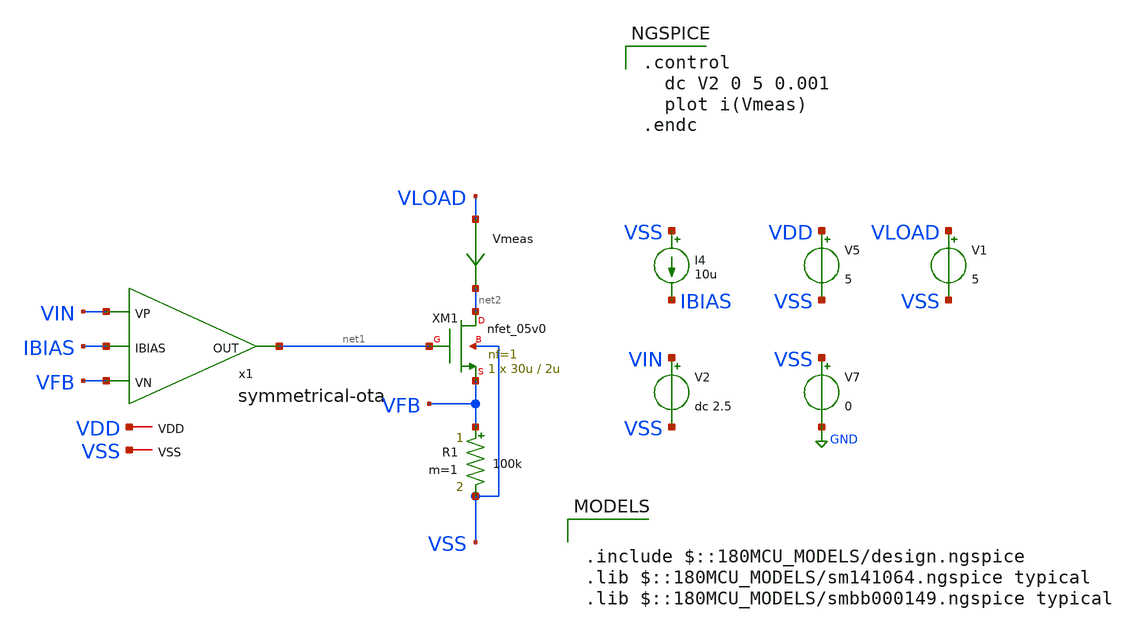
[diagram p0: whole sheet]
** sch_path: designs/vi-converter/vi-converter.sch
**.subckt vi-converter
x1 VDD VIN VFB IBIAS net1 VSS symmetrical-ota
XM1 net2 net1 VFB VSS nfet_05v0 L=2u W=30u nf=1 ad='int((nf+1)/2) * W/nf * 0.18u' as='int((nf+2)/2) * W/nf * 0.18u'
+ pd='2*int((nf+1)/2) * (W/nf + 0.18u)' ps='2*int((nf+2)/2) * (W/nf + 0.18u)' nrd='0.18u / W' nrs='0.18u / W'
+ sa=0 sb=0 sd=0 m=1
R1 VFB VSS 100k m=1
V2 VIN VSS dc 2.5
V5 VDD VSS 5
V7 VSS GND 0
I4 VSS IBIAS 10u
Vmeas VLOAD net2 0
.save i(vmeas)
V1 VLOAD VSS 5
**** begin user architecture code

.control
  dc V2 0 5 0.001
  plot i(Vmeas)
.endc




.include $::180MCU_MODELS/design.ngspice
.lib $::180MCU_MODELS/sm141064.ngspice typical
.lib $::180MCU_MODELS/smbb000149.ngspice typical

**** end user architecture code
**.ends

* expanding   symbol:
*+  /foss/designs/2026/buck-gf180-test/designs/symmetrical-ota/symmetrical-ota.sym # of pins=6
** sym_path: designs/symmetrical-ota/symmetrical-ota.sym
** sch_path: designs/symmetrical-ota/symmetrical-ota.sch
.subckt symmetrical-ota VDD VP VN IBIAS OUT VSS
*.ipin IBIAS
*.ipin VN
*.ipin VP
*.opin OUT
*.iopin VDD
*.iopin VSS
XM1 net3 VN net1 VDD pfet_05v0 L=0.9u W=10.5u nf=4 ad='int((nf+1)/2) * W/nf * 0.18u' as='int((nf+2)/2) * W/nf * 0.18u'
+ pd='2*int((nf+1)/2) * (W/nf + 0.18u)' ps='2*int((nf+2)/2) * (W/nf + 0.18u)' nrd='0.18u / W' nrs='0.18u / W'
+ sa=0 sb=0 sd=0 m=1
XM2 net2 VP net1 VDD pfet_05v0 L=0.9u W=10.5u nf=4 ad='int((nf+1)/2) * W/nf * 0.18u' as='int((nf+2)/2) * W/nf * 0.18u'
+ pd='2*int((nf+1)/2) * (W/nf + 0.18u)' ps='2*int((nf+2)/2) * (W/nf + 0.18u)' nrd='0.18u / W' nrs='0.18u / W'
+ sa=0 sb=0 sd=0 m=1
XM3 net1 IBIAS VDD VDD pfet_05v0 L=1u W=15u nf=4 ad='int((nf+1)/2) * W/nf * 0.18u' as='int((nf+2)/2) * W/nf * 0.18u'
+ pd='2*int((nf+1)/2) * (W/nf + 0.18u)' ps='2*int((nf+2)/2) * (W/nf + 0.18u)' nrd='0.18u / W' nrs='0.18u / W'
+ sa=0 sb=0 sd=0 m=1
XM4 IBIAS IBIAS VDD VDD pfet_05v0 L=1u W=15u nf=4 ad='int((nf+1)/2) * W/nf * 0.18u' as='int((nf+2)/2) * W/nf * 0.18u'
+ pd='2*int((nf+1)/2) * (W/nf + 0.18u)' ps='2*int((nf+2)/2) * (W/nf + 0.18u)' nrd='0.18u / W' nrs='0.18u / W'
+ sa=0 sb=0 sd=0 m=1
XM5 net2 net2 VSS VSS nfet_05v0 L=0.75u W=2.17u nf=1 ad='int((nf+1)/2) * W/nf * 0.18u' as='int((nf+2)/2) * W/nf * 0.18u'
+ pd='2*int((nf+1)/2) * (W/nf + 0.18u)' ps='2*int((nf+2)/2) * (W/nf + 0.18u)' nrd='0.18u / W' nrs='0.18u / W'
+ sa=0 sb=0 sd=0 m=1
XM6 net3 net3 VSS VSS nfet_05v0 L=0.75u W=2.17u nf=1 ad='int((nf+1)/2) * W/nf * 0.18u' as='int((nf+2)/2) * W/nf * 0.18u'
+ pd='2*int((nf+1)/2) * (W/nf + 0.18u)' ps='2*int((nf+2)/2) * (W/nf + 0.18u)' nrd='0.18u / W' nrs='0.18u / W'
+ sa=0 sb=0 sd=0 m=1
XM7 OUT net4 VDD VDD pfet_05v0 L=1u W=9.4u nf=4 ad='int((nf+1)/2) * W/nf * 0.18u' as='int((nf+2)/2) * W/nf * 0.18u'
+ pd='2*int((nf+1)/2) * (W/nf + 0.18u)' ps='2*int((nf+2)/2) * (W/nf + 0.18u)' nrd='0.18u / W' nrs='0.18u / W'
+ sa=0 sb=0 sd=0 m=1
XM8 net4 net4 VDD VDD pfet_05v0 L=1u W=9.4u nf=4 ad='int((nf+1)/2) * W/nf * 0.18u' as='int((nf+2)/2) * W/nf * 0.18u'
+ pd='2*int((nf+1)/2) * (W/nf + 0.18u)' ps='2*int((nf+2)/2) * (W/nf + 0.18u)' nrd='0.18u / W' nrs='0.18u / W'
+ sa=0 sb=0 sd=0 m=1
XM9 net4 net3 VSS VSS nfet_05v0 L=0.75u W=2.17u nf=1 ad='int((nf+1)/2) * W/nf * 0.18u' as='int((nf+2)/2) * W/nf * 0.18u'
+ pd='2*int((nf+1)/2) * (W/nf + 0.18u)' ps='2*int((nf+2)/2) * (W/nf + 0.18u)' nrd='0.18u / W' nrs='0.18u / W'
+ sa=0 sb=0 sd=0 m=1
XM10 OUT net2 VSS VSS nfet_05v0 L=0.75u W=2.17u nf=1 ad='int((nf+1)/2) * W/nf * 0.18u' as='int((nf+2)/2) * W/nf * 0.18u'
+ pd='2*int((nf+1)/2) * (W/nf + 0.18u)' ps='2*int((nf+2)/2) * (W/nf + 0.18u)' nrd='0.18u / W' nrs='0.18u / W'
+ sa=0 sb=0 sd=0 m=1
.ends

.GLOBAL GND
.end
